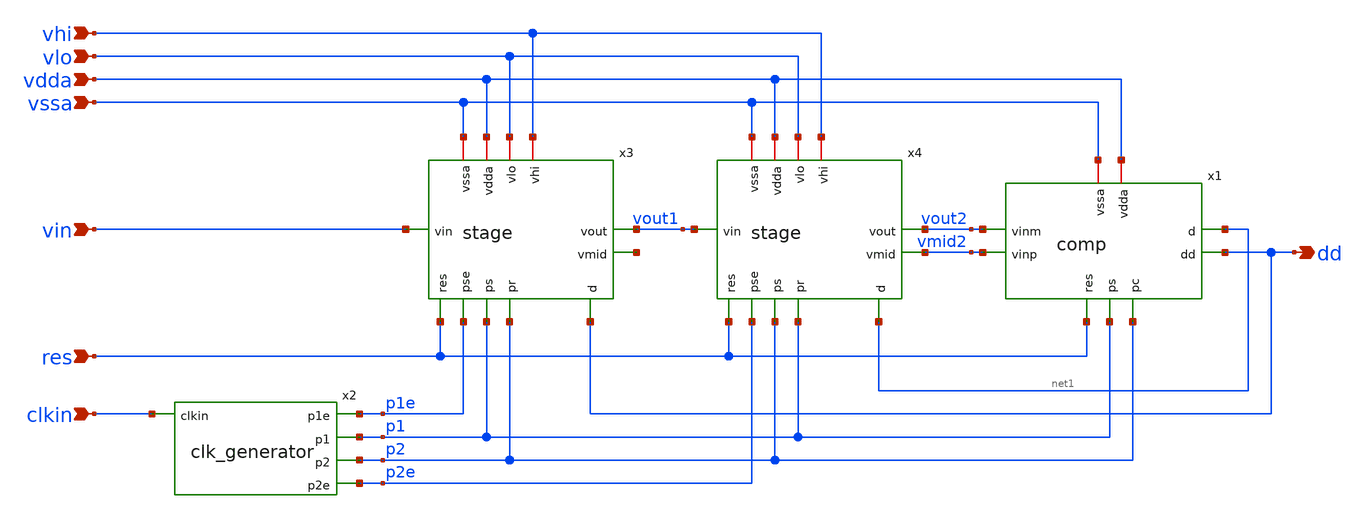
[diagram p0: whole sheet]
** sch_path: schematics/IDSM2.sch
**.subckt IDSM2 clkin res vin vssa vdda vlo vhi dd
*.ipin clkin
*.ipin res
*.ipin vin
*.ipin vssa
*.ipin vdda
*.ipin vlo
*.ipin vhi
*.opin dd
x1 p2 net1 dd vmid2 vssa p1 res vout2 vdda comp
x2 p1e clkin p1 p2 p2e clk_generator
x3 res p1e p1 p2 vin vout1 vssa dd net2 vdda vhi vlo stage
x4 res p2e p2 p1 vout1 vout2 vssa net1 vmid2 vdda vhi vlo stage
**.ends
.end
